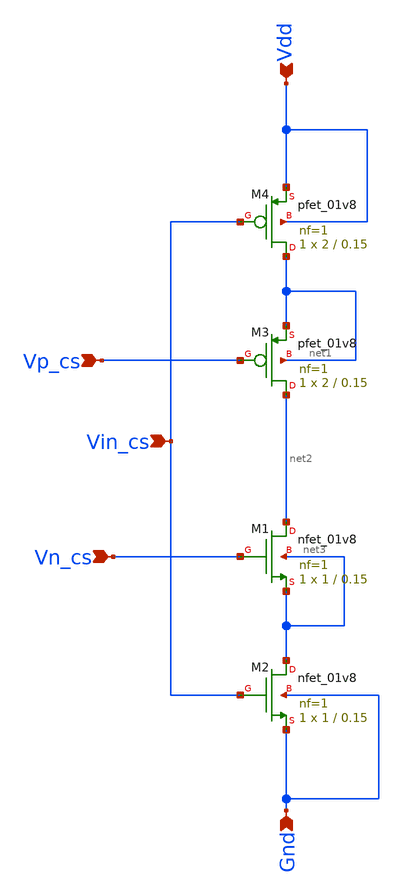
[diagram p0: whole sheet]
** sch_path: cs_inv.sch
**.subckt cs_inv Gnd Vdd Vp_cs Vn_cs Vin_cs
*.ipin Gnd
*.ipin Vdd
*.ipin Vp_cs
*.ipin Vn_cs
*.ipin Vin_cs
XM1 net2 Vn_cs net3 net3 sky130_fd_pr__nfet_01v8 L=0.15 W=1 nf=1 ad='int((nf+1)/2) * W/nf * 0.29' as='int((nf+2)/2) * W/nf * 0.29'
+ pd='2*int((nf+1)/2) * (W/nf + 0.29)' ps='2*int((nf+2)/2) * (W/nf + 0.29)' nrd='0.29 / W' nrs='0.29 / W'
+ sa=0 sb=0 sd=0 mult=1 m=1
XM2 net3 Vin_cs Gnd Gnd sky130_fd_pr__nfet_01v8 L=0.15 W=1 nf=1 ad='int((nf+1)/2) * W/nf * 0.29' as='int((nf+2)/2) * W/nf * 0.29'
+ pd='2*int((nf+1)/2) * (W/nf + 0.29)' ps='2*int((nf+2)/2) * (W/nf + 0.29)' nrd='0.29 / W' nrs='0.29 / W'
+ sa=0 sb=0 sd=0 mult=1 m=1
XM3 net2 Vp_cs net1 net1 sky130_fd_pr__pfet_01v8 L=0.15 W=2 nf=1 ad='int((nf+1)/2) * W/nf * 0.29' as='int((nf+2)/2) * W/nf * 0.29'
+ pd='2*int((nf+1)/2) * (W/nf + 0.29)' ps='2*int((nf+2)/2) * (W/nf + 0.29)' nrd='0.29 / W' nrs='0.29 / W'
+ sa=0 sb=0 sd=0 mult=1 m=1
XM4 net1 Vin_cs Vdd Vdd sky130_fd_pr__pfet_01v8 L=0.15 W=2 nf=1 ad='int((nf+1)/2) * W/nf * 0.29' as='int((nf+2)/2) * W/nf * 0.29'
+ pd='2*int((nf+1)/2) * (W/nf + 0.29)' ps='2*int((nf+2)/2) * (W/nf + 0.29)' nrd='0.29 / W' nrs='0.29 / W'
+ sa=0 sb=0 sd=0 mult=1 m=1
**.ends
.end
